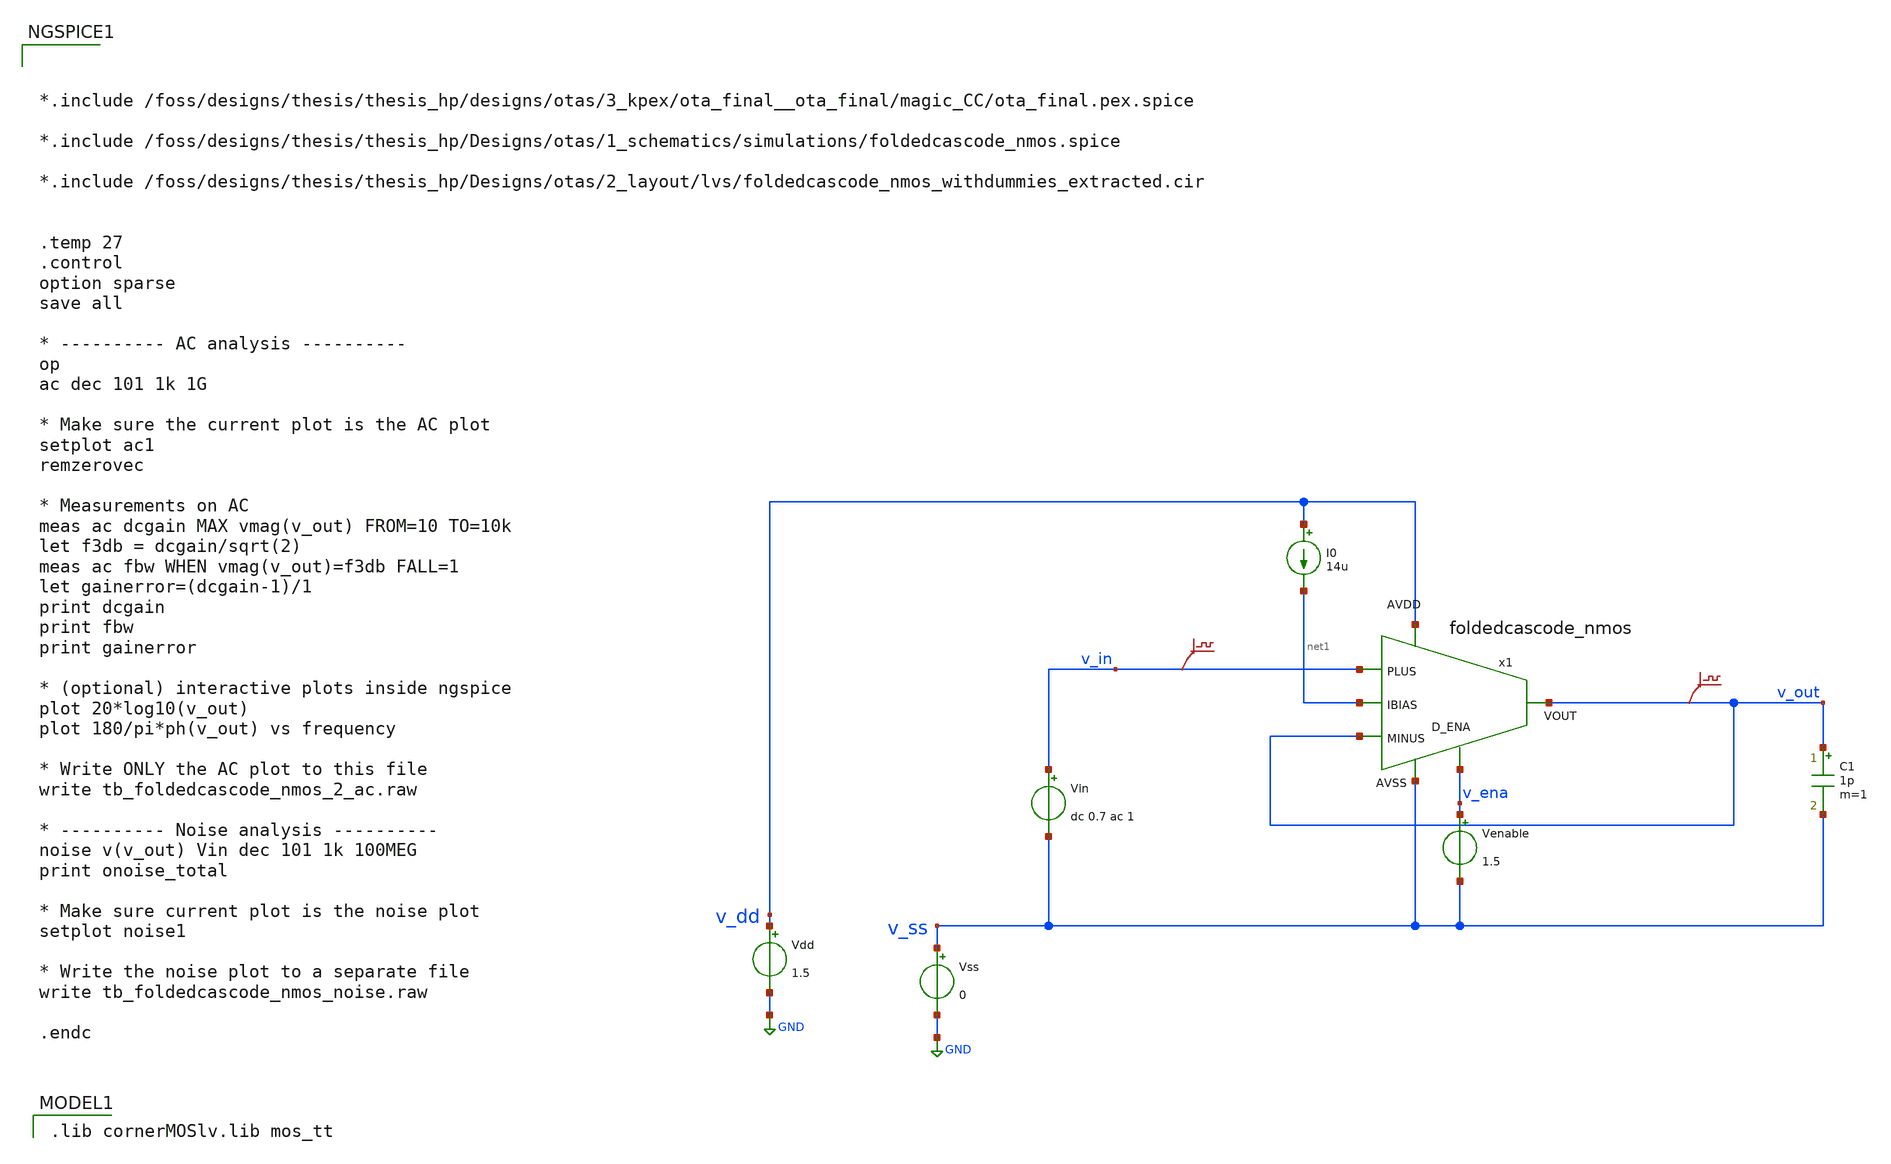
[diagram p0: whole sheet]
** sch_path: Designs/otas/1_schematics/tb_foldedcascode_nmos_ac.sch
* (c) 2025 Thesis_HP, Apache-2.0 license
**.subckt tb_foldedcascode_nmos_ac
Vss v_ss GND 0
Vdd v_dd GND 1.5
Vin v_in v_ss dc 0.7 ac 1
.save v(v_in)
I0 v_dd net1 14u
C1 v_out v_ss 1p m=1
.save v(v_out)
Venable v_ena v_ss 1.5
x1 v_dd net1 v_out v_out v_in v_ena v_ss foldedcascode_nmos
**** begin user architecture code
 .lib cornerMOSlv.lib mos_tt




*.include /foss/designs/thesis/thesis_hp/designs/otas/3_kpex/ota_final__ota_final/magic_CC/ota_final.pex.spice

*.include /foss/designs/thesis/thesis_hp/Designs/otas/1_schematics/simulations/foldedcascode_nmos.spice

*.include /foss/designs/thesis/thesis_hp/Designs/otas/2_layout/lvs/foldedcascode_nmos_withdummies_extracted.cir


.temp 27
.control
option sparse
save all

* ---------- AC analysis ----------
op
ac dec 101 1k 1G

* Make sure the current plot is the AC plot
setplot ac1
remzerovec

* Measurements on AC
meas ac dcgain MAX vmag(v_out) FROM=10 TO=10k
let f3db = dcgain/sqrt(2)
meas ac fbw WHEN vmag(v_out)=f3db FALL=1
let gainerror=(dcgain-1)/1
print dcgain
print fbw
print gainerror

* (optional) interactive plots inside ngspice
plot 20*log10(v_out)
plot 180/pi*ph(v_out) vs frequency

* Write ONLY the AC plot to this file
write tb_foldedcascode_nmos_2_ac.raw

* ---------- Noise analysis ----------
noise v(v_out) Vin dec 101 1k 100MEG
print onoise_total

* Make sure current plot is the noise plot
setplot noise1

* Write the noise plot to a separate file
write tb_foldedcascode_nmos_noise.raw

.endc


**** end user architecture code
**.ends
.GLOBAL GND
.end
